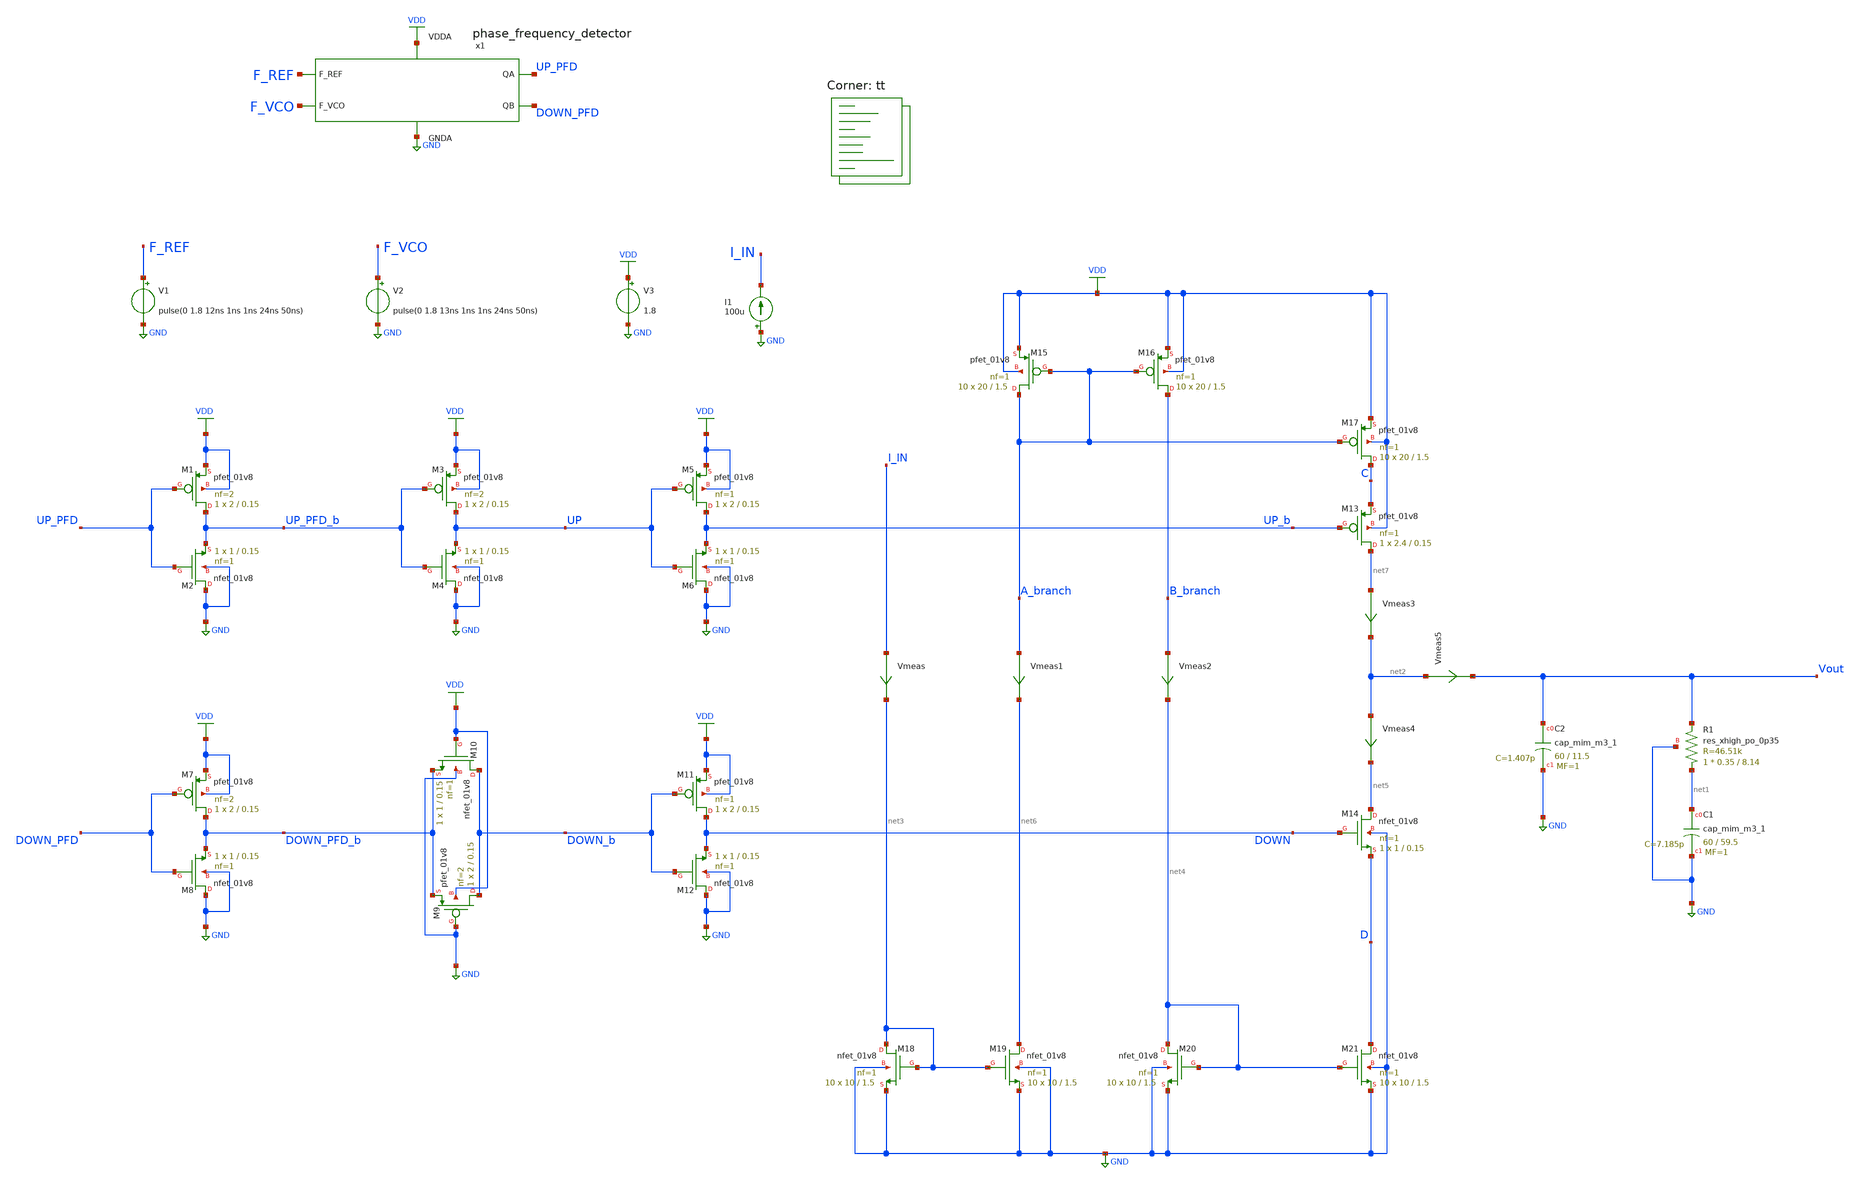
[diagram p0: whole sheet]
** sch_path: projects/pll/charge_pump/xschem_ngspice/pfd_charge_pump_3.sch
**.subckt pfd_charge_pump_3
V3 VDD GND 1.8
XC2 Vout GND sky130_fd_pr__cap_mim_m3_1 W=60 L=11.5 MF=1 m=1
XC1 net1 GND sky130_fd_pr__cap_mim_m3_1 W=60 L=59.5 MF=1 m=1
V1 F_REF GND pulse(0 1.8 12ns 1ns 1ns 24ns 50ns)
V2 F_VCO GND pulse(0 1.8 13ns 1ns 1ns 24ns 50ns)
x1 F_REF F_VCO VDD UP_PFD DOWN_PFD GND phase_frequency_detector
XR1 net1 Vout GND sky130_fd_pr__res_xhigh_po_0p35 L=8.14 mult=1 m=1
I1 GND I_IN 100u
Vmeas5 net2 Vout 0
.save i(vmeas5)
XM18 net3 net3 GND GND sky130_fd_pr__nfet_01v8 L=1.5 W=10 nf=1 ad='int((nf+1)/2) * W/nf * 0.29' as='int((nf+2)/2) * W/nf * 0.29'
+ pd='2*int((nf+1)/2) * (W/nf + 0.29)' ps='2*int((nf+2)/2) * (W/nf + 0.29)' nrd='0.29 / W' nrs='0.29 / W'
+ sa=0 sb=0 sd=0 mult=10 m=10
XM19 net6 net3 GND GND sky130_fd_pr__nfet_01v8 L=1.5 W=10 nf=1 ad='int((nf+1)/2) * W/nf * 0.29' as='int((nf+2)/2) * W/nf * 0.29'
+ pd='2*int((nf+1)/2) * (W/nf + 0.29)' ps='2*int((nf+2)/2) * (W/nf + 0.29)' nrd='0.29 / W' nrs='0.29 / W'
+ sa=0 sb=0 sd=0 mult=10 m=10
Vmeas I_IN net3 0
.save i(vmeas)
XM13 net7 UP_b C VDD sky130_fd_pr__pfet_01v8 L=0.15 W=2.4 nf=1 ad='int((nf+1)/2) * W/nf * 0.29' as='int((nf+2)/2) * W/nf * 0.29'
+ pd='2*int((nf+1)/2) * (W/nf + 0.29)' ps='2*int((nf+2)/2) * (W/nf + 0.29)' nrd='0.29 / W' nrs='0.29 / W'
+ sa=0 sb=0 sd=0 mult=1 m=1
Vmeas3 net7 net2 0
.save i(vmeas3)
Vmeas4 net2 net5 0
.save i(vmeas4)
XM14 net5 DOWN D GND sky130_fd_pr__nfet_01v8 L=0.15 W=1 nf=1 ad='int((nf+1)/2) * W/nf * 0.29' as='int((nf+2)/2) * W/nf * 0.29'
+ pd='2*int((nf+1)/2) * (W/nf + 0.29)' ps='2*int((nf+2)/2) * (W/nf + 0.29)' nrd='0.29 / W' nrs='0.29 / W'
+ sa=0 sb=0 sd=0 mult=1 m=1
XM17 C A_branch VDD VDD sky130_fd_pr__pfet_01v8 L=1.5 W=20 nf=1 ad='int((nf+1)/2) * W/nf * 0.29' as='int((nf+2)/2) * W/nf * 0.29'
+ pd='2*int((nf+1)/2) * (W/nf + 0.29)' ps='2*int((nf+2)/2) * (W/nf + 0.29)' nrd='0.29 / W' nrs='0.29 / W'
+ sa=0 sb=0 sd=0 mult=10 m=10
XM21 D net4 GND GND sky130_fd_pr__nfet_01v8 L=1.5 W=10 nf=1 ad='int((nf+1)/2) * W/nf * 0.29' as='int((nf+2)/2) * W/nf * 0.29'
+ pd='2*int((nf+1)/2) * (W/nf + 0.29)' ps='2*int((nf+2)/2) * (W/nf + 0.29)' nrd='0.29 / W' nrs='0.29 / W'
+ sa=0 sb=0 sd=0 mult=10 m=10
XM20 net4 net4 GND GND sky130_fd_pr__nfet_01v8 L=1.5 W=10 nf=1 ad='int((nf+1)/2) * W/nf * 0.29' as='int((nf+2)/2) * W/nf * 0.29'
+ pd='2*int((nf+1)/2) * (W/nf + 0.29)' ps='2*int((nf+2)/2) * (W/nf + 0.29)' nrd='0.29 / W' nrs='0.29 / W'
+ sa=0 sb=0 sd=0 mult=10 m=10
XM15 A_branch A_branch VDD VDD sky130_fd_pr__pfet_01v8 L=1.5 W=20 nf=1 ad='int((nf+1)/2) * W/nf * 0.29'
+ as='int((nf+2)/2) * W/nf * 0.29' pd='2*int((nf+1)/2) * (W/nf + 0.29)' ps='2*int((nf+2)/2) * (W/nf + 0.29)'
+ nrd='0.29 / W' nrs='0.29 / W' sa=0 sb=0 sd=0 mult=10 m=10
XM16 B_branch A_branch VDD VDD sky130_fd_pr__pfet_01v8 L=1.5 W=20 nf=1 ad='int((nf+1)/2) * W/nf * 0.29'
+ as='int((nf+2)/2) * W/nf * 0.29' pd='2*int((nf+1)/2) * (W/nf + 0.29)' ps='2*int((nf+2)/2) * (W/nf + 0.29)'
+ nrd='0.29 / W' nrs='0.29 / W' sa=0 sb=0 sd=0 mult=10 m=10
Vmeas1 A_branch net6 0
.save i(vmeas1)
Vmeas2 B_branch net4 0
.save i(vmeas2)
XM9 DOWN_b GND DOWN_PFD_b VDD sky130_fd_pr__pfet_01v8 L=0.15 W=2 nf=2 ad='int((nf+1)/2) * W/nf * 0.29'
+ as='int((nf+2)/2) * W/nf * 0.29' pd='2*int((nf+1)/2) * (W/nf + 0.29)' ps='2*int((nf+2)/2) * (W/nf + 0.29)'
+ nrd='0.29 / W' nrs='0.29 / W' sa=0 sb=0 sd=0 mult=1 m=1
XM10 DOWN_b VDD DOWN_PFD_b GND sky130_fd_pr__nfet_01v8 L=0.15 W=1 nf=1 ad='int((nf+1)/2) * W/nf * 0.29'
+ as='int((nf+2)/2) * W/nf * 0.29' pd='2*int((nf+1)/2) * (W/nf + 0.29)' ps='2*int((nf+2)/2) * (W/nf + 0.29)'
+ nrd='0.29 / W' nrs='0.29 / W' sa=0 sb=0 sd=0 mult=1 m=1
XM1 UP_PFD_b UP_PFD VDD VDD sky130_fd_pr__pfet_01v8 L=0.15 W=2 nf=2 ad='int((nf+1)/2) * W/nf * 0.29'
+ as='int((nf+2)/2) * W/nf * 0.29' pd='2*int((nf+1)/2) * (W/nf + 0.29)' ps='2*int((nf+2)/2) * (W/nf + 0.29)'
+ nrd='0.29 / W' nrs='0.29 / W' sa=0 sb=0 sd=0 mult=1 m=1
XM2 GND UP_PFD UP_PFD_b GND sky130_fd_pr__nfet_01v8 L=0.15 W=1 nf=1 ad='int((nf+1)/2) * W/nf * 0.29'
+ as='int((nf+2)/2) * W/nf * 0.29' pd='2*int((nf+1)/2) * (W/nf + 0.29)' ps='2*int((nf+2)/2) * (W/nf + 0.29)'
+ nrd='0.29 / W' nrs='0.29 / W' sa=0 sb=0 sd=0 mult=1 m=1
XM7 DOWN_PFD_b DOWN_PFD VDD VDD sky130_fd_pr__pfet_01v8 L=0.15 W=2 nf=2 ad='int((nf+1)/2) * W/nf * 0.29'
+ as='int((nf+2)/2) * W/nf * 0.29' pd='2*int((nf+1)/2) * (W/nf + 0.29)' ps='2*int((nf+2)/2) * (W/nf + 0.29)'
+ nrd='0.29 / W' nrs='0.29 / W' sa=0 sb=0 sd=0 mult=1 m=1
XM8 GND DOWN_PFD DOWN_PFD_b GND sky130_fd_pr__nfet_01v8 L=0.15 W=1 nf=1 ad='int((nf+1)/2) * W/nf * 0.29'
+ as='int((nf+2)/2) * W/nf * 0.29' pd='2*int((nf+1)/2) * (W/nf + 0.29)' ps='2*int((nf+2)/2) * (W/nf + 0.29)'
+ nrd='0.29 / W' nrs='0.29 / W' sa=0 sb=0 sd=0 mult=1 m=1
XM3 UP UP_PFD_b VDD VDD sky130_fd_pr__pfet_01v8 L=0.15 W=2 nf=2 ad='int((nf+1)/2) * W/nf * 0.29' as='int((nf+2)/2) * W/nf * 0.29'
+ pd='2*int((nf+1)/2) * (W/nf + 0.29)' ps='2*int((nf+2)/2) * (W/nf + 0.29)' nrd='0.29 / W' nrs='0.29 / W'
+ sa=0 sb=0 sd=0 mult=1 m=1
XM4 GND UP_PFD_b UP GND sky130_fd_pr__nfet_01v8 L=0.15 W=1 nf=1 ad='int((nf+1)/2) * W/nf * 0.29' as='int((nf+2)/2) * W/nf * 0.29'
+ pd='2*int((nf+1)/2) * (W/nf + 0.29)' ps='2*int((nf+2)/2) * (W/nf + 0.29)' nrd='0.29 / W' nrs='0.29 / W'
+ sa=0 sb=0 sd=0 mult=1 m=1
XM5 UP_b UP VDD VDD sky130_fd_pr__pfet_01v8 L=0.15 W=2 nf=1 ad='int((nf+1)/2) * W/nf * 0.29' as='int((nf+2)/2) * W/nf * 0.29'
+ pd='2*int((nf+1)/2) * (W/nf + 0.29)' ps='2*int((nf+2)/2) * (W/nf + 0.29)' nrd='0.29 / W' nrs='0.29 / W'
+ sa=0 sb=0 sd=0 mult=1 m=1
XM6 GND UP UP_b GND sky130_fd_pr__nfet_01v8 L=0.15 W=1 nf=1 ad='int((nf+1)/2) * W/nf * 0.29' as='int((nf+2)/2) * W/nf * 0.29'
+ pd='2*int((nf+1)/2) * (W/nf + 0.29)' ps='2*int((nf+2)/2) * (W/nf + 0.29)' nrd='0.29 / W' nrs='0.29 / W'
+ sa=0 sb=0 sd=0 mult=1 m=1
XM11 DOWN DOWN_b VDD VDD sky130_fd_pr__pfet_01v8 L=0.15 W=2 nf=1 ad='int((nf+1)/2) * W/nf * 0.29' as='int((nf+2)/2) * W/nf * 0.29'
+ pd='2*int((nf+1)/2) * (W/nf + 0.29)' ps='2*int((nf+2)/2) * (W/nf + 0.29)' nrd='0.29 / W' nrs='0.29 / W'
+ sa=0 sb=0 sd=0 mult=1 m=1
XM12 GND DOWN_b DOWN GND sky130_fd_pr__nfet_01v8 L=0.15 W=1 nf=1 ad='int((nf+1)/2) * W/nf * 0.29' as='int((nf+2)/2) * W/nf * 0.29'
+ pd='2*int((nf+1)/2) * (W/nf + 0.29)' ps='2*int((nf+2)/2) * (W/nf + 0.29)' nrd='0.29 / W' nrs='0.29 / W'
+ sa=0 sb=0 sd=0 mult=1 m=1
**** begin user architecture code
.lib $::SKYWATER_MODELS/sky130.lib.spice tt



.include /foss/pdks/sky130A/libs.ref/sky130_fd_sc_hd/spice/sky130_fd_sc_hd.spice

.option method=gear
.option wnflag=1
.option savecurrents

* V_out initial voltage value for the F_VCO delay of 22ns (lagging)
* .ic v(vout) = 0

* V_out initial voltage value for the F_VCO delay of 2ns  (leading)
* .ic v(vout) = 1.8

* V_out initial voltage value for the F_VCO delay of 12ns (lock condition)
.ic v(vout) = 0.83

.control
  save v(f_ref) save v(f_vco) save v(up_pfd) v(down_pfd) v(up_pfd_b) v(down_pfd_b) v(up) v(up_b)
+ v(down) v(down_b) v(a_branch) v(b_branch) v(c) v(d) v(vout)

  * timestep for exact simulation results
  tran 5ps 0.5us

  * timestep for faster simulation results
  * tran 50ps 0.5us

  remzerovec
  write pfd_charge_pump_3.raw
  set appendwrite
.endc



**** end user architecture code
**.ends
.GLOBAL GND
.GLOBAL VDD
.end
